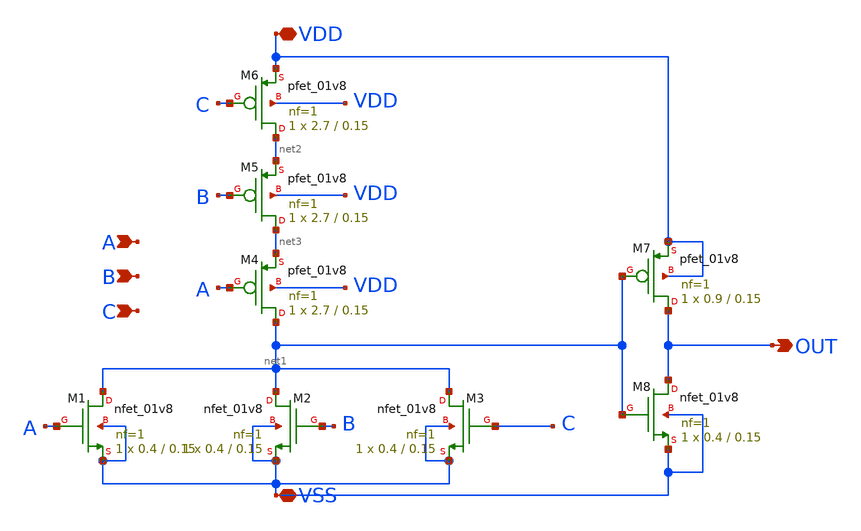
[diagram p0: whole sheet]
** sch_path: design/OR3/xschem/or3.sch
**.subckt or3 A B VSS VDD OUT C
*.ipin A
*.ipin B
*.iopin VSS
*.iopin VDD
*.opin OUT
*.ipin C
XM4 net1 A net3 VDD sky130_fd_pr__pfet_01v8 L=0.15 W=2.7 nf=1 ad='int((nf+1)/2) * W/nf * 0.29' as='int((nf+2)/2) * W/nf * 0.29'
+ pd='2*int((nf+1)/2) * (W/nf + 0.29)' ps='2*int((nf+2)/2) * (W/nf + 0.29)' nrd='0.29 / W' nrs='0.29 / W'
+ sa=0 sb=0 sd=0 mult=1 m=1
XM6 net2 C VDD VDD sky130_fd_pr__pfet_01v8 L=0.15 W=2.7 nf=1 ad='int((nf+1)/2) * W/nf * 0.29' as='int((nf+2)/2) * W/nf * 0.29'
+ pd='2*int((nf+1)/2) * (W/nf + 0.29)' ps='2*int((nf+2)/2) * (W/nf + 0.29)' nrd='0.29 / W' nrs='0.29 / W'
+ sa=0 sb=0 sd=0 mult=1 m=1
XM1 net1 A VSS VSS sky130_fd_pr__nfet_01v8 L=0.15 W=0.4 nf=1 ad='int((nf+1)/2) * W/nf * 0.29' as='int((nf+2)/2) * W/nf * 0.29'
+ pd='2*int((nf+1)/2) * (W/nf + 0.29)' ps='2*int((nf+2)/2) * (W/nf + 0.29)' nrd='0.29 / W' nrs='0.29 / W'
+ sa=0 sb=0 sd=0 mult=1 m=1
XM2 net1 B VSS VSS sky130_fd_pr__nfet_01v8 L=0.15 W=0.4 nf=1 ad='int((nf+1)/2) * W/nf * 0.29' as='int((nf+2)/2) * W/nf * 0.29'
+ pd='2*int((nf+1)/2) * (W/nf + 0.29)' ps='2*int((nf+2)/2) * (W/nf + 0.29)' nrd='0.29 / W' nrs='0.29 / W'
+ sa=0 sb=0 sd=0 mult=1 m=1
XM5 net3 B net2 VDD sky130_fd_pr__pfet_01v8 L=0.15 W=2.7 nf=1 ad='int((nf+1)/2) * W/nf * 0.29' as='int((nf+2)/2) * W/nf * 0.29'
+ pd='2*int((nf+1)/2) * (W/nf + 0.29)' ps='2*int((nf+2)/2) * (W/nf + 0.29)' nrd='0.29 / W' nrs='0.29 / W'
+ sa=0 sb=0 sd=0 mult=1 m=1
XM3 net1 C VSS VSS sky130_fd_pr__nfet_01v8 L=0.15 W=0.4 nf=1 ad='int((nf+1)/2) * W/nf * 0.29' as='int((nf+2)/2) * W/nf * 0.29'
+ pd='2*int((nf+1)/2) * (W/nf + 0.29)' ps='2*int((nf+2)/2) * (W/nf + 0.29)' nrd='0.29 / W' nrs='0.29 / W'
+ sa=0 sb=0 sd=0 mult=1 m=1
XM7 OUT net1 VDD VDD sky130_fd_pr__pfet_01v8 L=0.15 W=0.9 nf=1 ad='int((nf+1)/2) * W/nf * 0.29' as='int((nf+2)/2) * W/nf * 0.29'
+ pd='2*int((nf+1)/2) * (W/nf + 0.29)' ps='2*int((nf+2)/2) * (W/nf + 0.29)' nrd='0.29 / W' nrs='0.29 / W'
+ sa=0 sb=0 sd=0 mult=1 m=1
XM8 OUT net1 VSS VSS sky130_fd_pr__nfet_01v8 L=0.15 W=0.4 nf=1 ad='int((nf+1)/2) * W/nf * 0.29' as='int((nf+2)/2) * W/nf * 0.29'
+ pd='2*int((nf+1)/2) * (W/nf + 0.29)' ps='2*int((nf+2)/2) * (W/nf + 0.29)' nrd='0.29 / W' nrs='0.29 / W'
+ sa=0 sb=0 sd=0 mult=1 m=1
**.ends
.end
